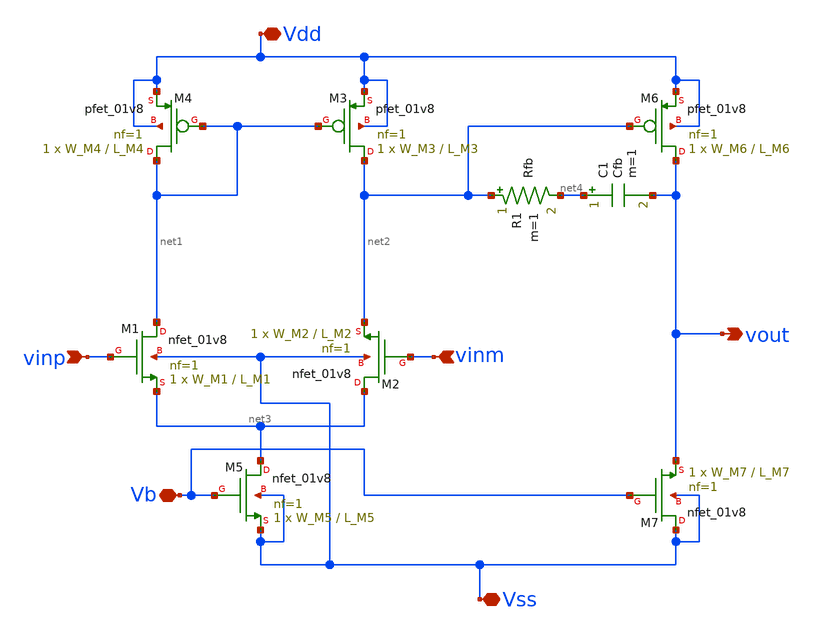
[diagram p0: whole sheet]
** sch_path: xschem/two_stage.sch
**.subckt two_stage Vdd vinm vinp Vb vout Vss
*.iopin Vdd
*.ipin vinm
*.ipin vinp
*.iopin Vb
*.opin vout
*.iopin Vss
XM1 net1 vinp net3 Vss sky130_fd_pr__nfet_01v8 L=L_M1 W=W_M1 nf=1 ad='int((nf+1)/2) * W/nf * 0.29' as='int((nf+2)/2) * W/nf * 0.29'
+ pd='2*int((nf+1)/2) * (W/nf + 0.29)' ps='2*int((nf+2)/2) * (W/nf + 0.29)' nrd='0.29 / W' nrs='0.29 / W'
+ sa=0 sb=0 sd=0 mult=1 m=1
XM2 net3 vinm net2 Vss sky130_fd_pr__nfet_01v8 L=L_M2 W=W_M2 nf=1 ad='int((nf+1)/2) * W/nf * 0.29' as='int((nf+2)/2) * W/nf * 0.29'
+ pd='2*int((nf+1)/2) * (W/nf + 0.29)' ps='2*int((nf+2)/2) * (W/nf + 0.29)' nrd='0.29 / W' nrs='0.29 / W'
+ sa=0 sb=0 sd=0 mult=1 m=1
XM3 net2 net1 Vdd Vdd sky130_fd_pr__pfet_01v8 L=L_M3 W=W_M3 nf=1 ad='int((nf+1)/2) * W/nf * 0.29' as='int((nf+2)/2) * W/nf * 0.29'
+ pd='2*int((nf+1)/2) * (W/nf + 0.29)' ps='2*int((nf+2)/2) * (W/nf + 0.29)' nrd='0.29 / W' nrs='0.29 / W'
+ sa=0 sb=0 sd=0 mult=1 m=1
XM4 net1 net1 Vdd Vdd sky130_fd_pr__pfet_01v8 L=L_M4 W=W_M4 nf=1 ad='int((nf+1)/2) * W/nf * 0.29' as='int((nf+2)/2) * W/nf * 0.29'
+ pd='2*int((nf+1)/2) * (W/nf + 0.29)' ps='2*int((nf+2)/2) * (W/nf + 0.29)' nrd='0.29 / W' nrs='0.29 / W'
+ sa=0 sb=0 sd=0 mult=1 m=1
XM5 net3 Vb Vss Vss sky130_fd_pr__nfet_01v8 L=L_M5 W=W_M5 nf=1 ad='int((nf+1)/2) * W/nf * 0.29' as='int((nf+2)/2) * W/nf * 0.29'
+ pd='2*int((nf+1)/2) * (W/nf + 0.29)' ps='2*int((nf+2)/2) * (W/nf + 0.29)' nrd='0.29 / W' nrs='0.29 / W'
+ sa=0 sb=0 sd=0 mult=1 m=1
XM6 vout net2 Vdd Vdd sky130_fd_pr__pfet_01v8 L=L_M6 W=W_M6 nf=1 ad='int((nf+1)/2) * W/nf * 0.29' as='int((nf+2)/2) * W/nf * 0.29'
+ pd='2*int((nf+1)/2) * (W/nf + 0.29)' ps='2*int((nf+2)/2) * (W/nf + 0.29)' nrd='0.29 / W' nrs='0.29 / W'
+ sa=0 sb=0 sd=0 mult=1 m=1
XM7 Vss Vb vout Vss sky130_fd_pr__nfet_01v8 L=L_M7 W=W_M7 nf=1 ad='int((nf+1)/2) * W/nf * 0.29' as='int((nf+2)/2) * W/nf * 0.29'
+ pd='2*int((nf+1)/2) * (W/nf + 0.29)' ps='2*int((nf+2)/2) * (W/nf + 0.29)' nrd='0.29 / W' nrs='0.29 / W'
+ sa=0 sb=0 sd=0 mult=1 m=1
R1 net2 net4 Rfb m=1
C1 net4 vout Cfb m=1
**.ends
.end
